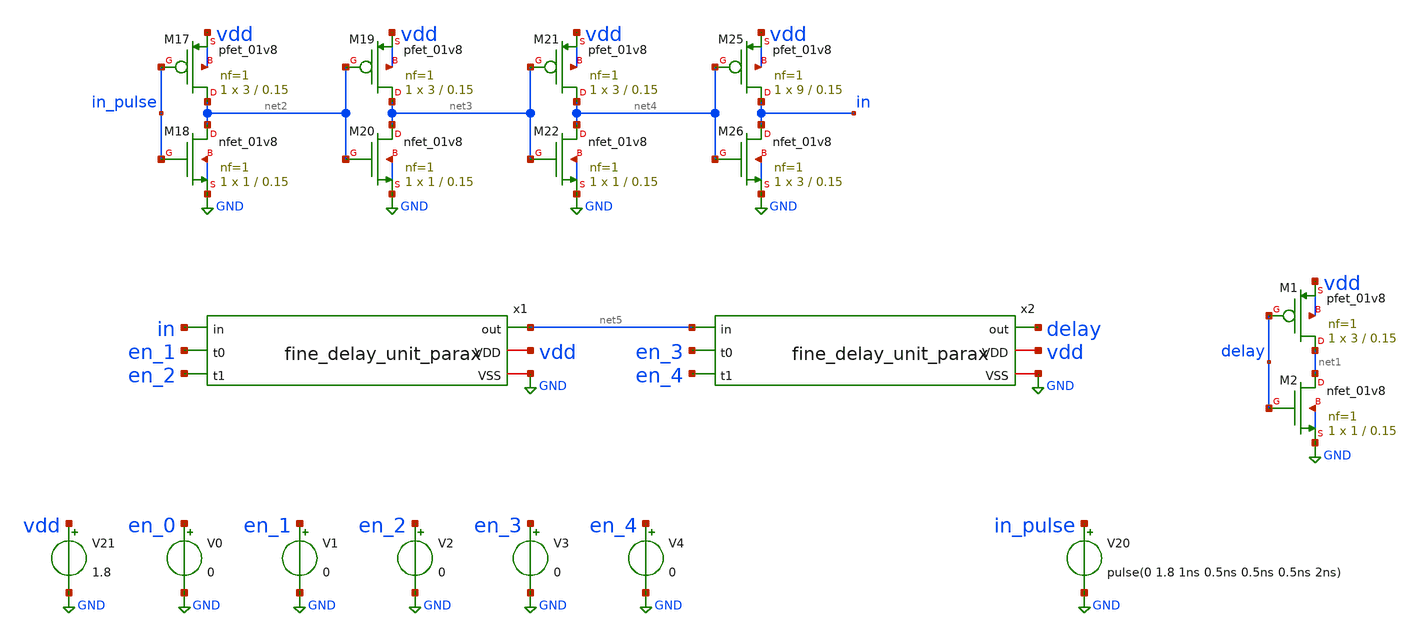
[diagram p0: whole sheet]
** sch_path: xschem/fine_delay_parax_tb.sch
**.subckt fine_delay_parax_tb
V21 vdd GND 1.8
V20 in_pulse GND pulse(0 1.8 1ns 0.5ns 0.5ns 0.5ns 2ns)
XM1 net1 delay vdd vdd sky130_fd_pr__pfet_01v8 L=0.15 W=3 nf=1 ad='int((nf+1)/2) * W/nf * 0.29' as='int((nf+2)/2) * W/nf * 0.29'
+ pd='2*int((nf+1)/2) * (W/nf + 0.29)' ps='2*int((nf+2)/2) * (W/nf + 0.29)' nrd='0.29 / W' nrs='0.29 / W'
+ sa=0 sb=0 sd=0 mult=1 m=1
XM2 net1 delay GND GND sky130_fd_pr__nfet_01v8 L=0.15 W=1 nf=1 ad='int((nf+1)/2) * W/nf * 0.29' as='int((nf+2)/2) * W/nf * 0.29'
+ pd='2*int((nf+1)/2) * (W/nf + 0.29)' ps='2*int((nf+2)/2) * (W/nf + 0.29)' nrd='0.29 / W' nrs='0.29 / W'
+ sa=0 sb=0 sd=0 mult=1 m=1
V0 en_0 GND 0
V1 en_1 GND 0
V2 en_2 GND 0
V3 en_3 GND 0
XM17 net2 in_pulse vdd vdd sky130_fd_pr__pfet_01v8 L=0.15 W=3 nf=1 ad='int((nf+1)/2) * W/nf * 0.29' as='int((nf+2)/2) * W/nf * 0.29'
+ pd='2*int((nf+1)/2) * (W/nf + 0.29)' ps='2*int((nf+2)/2) * (W/nf + 0.29)' nrd='0.29 / W' nrs='0.29 / W'
+ sa=0 sb=0 sd=0 mult=1 m=1
XM18 net2 in_pulse GND GND sky130_fd_pr__nfet_01v8 L=0.15 W=1 nf=1 ad='int((nf+1)/2) * W/nf * 0.29' as='int((nf+2)/2) * W/nf * 0.29'
+ pd='2*int((nf+1)/2) * (W/nf + 0.29)' ps='2*int((nf+2)/2) * (W/nf + 0.29)' nrd='0.29 / W' nrs='0.29 / W'
+ sa=0 sb=0 sd=0 mult=1 m=1
XM19 net3 net2 vdd vdd sky130_fd_pr__pfet_01v8 L=0.15 W=3 nf=1 ad='int((nf+1)/2) * W/nf * 0.29' as='int((nf+2)/2) * W/nf * 0.29'
+ pd='2*int((nf+1)/2) * (W/nf + 0.29)' ps='2*int((nf+2)/2) * (W/nf + 0.29)' nrd='0.29 / W' nrs='0.29 / W'
+ sa=0 sb=0 sd=0 mult=1 m=1
XM20 net3 net2 GND GND sky130_fd_pr__nfet_01v8 L=0.15 W=1 nf=1 ad='int((nf+1)/2) * W/nf * 0.29' as='int((nf+2)/2) * W/nf * 0.29'
+ pd='2*int((nf+1)/2) * (W/nf + 0.29)' ps='2*int((nf+2)/2) * (W/nf + 0.29)' nrd='0.29 / W' nrs='0.29 / W'
+ sa=0 sb=0 sd=0 mult=1 m=1
XM21 net4 net3 vdd vdd sky130_fd_pr__pfet_01v8 L=0.15 W=3 nf=1 ad='int((nf+1)/2) * W/nf * 0.29' as='int((nf+2)/2) * W/nf * 0.29'
+ pd='2*int((nf+1)/2) * (W/nf + 0.29)' ps='2*int((nf+2)/2) * (W/nf + 0.29)' nrd='0.29 / W' nrs='0.29 / W'
+ sa=0 sb=0 sd=0 mult=1 m=1
XM22 net4 net3 GND GND sky130_fd_pr__nfet_01v8 L=0.15 W=1 nf=1 ad='int((nf+1)/2) * W/nf * 0.29' as='int((nf+2)/2) * W/nf * 0.29'
+ pd='2*int((nf+1)/2) * (W/nf + 0.29)' ps='2*int((nf+2)/2) * (W/nf + 0.29)' nrd='0.29 / W' nrs='0.29 / W'
+ sa=0 sb=0 sd=0 mult=1 m=1
XM25 in net4 vdd vdd sky130_fd_pr__pfet_01v8 L=0.15 W=9 nf=1 ad='int((nf+1)/2) * W/nf * 0.29' as='int((nf+2)/2) * W/nf * 0.29'
+ pd='2*int((nf+1)/2) * (W/nf + 0.29)' ps='2*int((nf+2)/2) * (W/nf + 0.29)' nrd='0.29 / W' nrs='0.29 / W'
+ sa=0 sb=0 sd=0 mult=1 m=1
XM26 in net4 GND GND sky130_fd_pr__nfet_01v8 L=0.15 W=3 nf=1 ad='int((nf+1)/2) * W/nf * 0.29' as='int((nf+2)/2) * W/nf * 0.29'
+ pd='2*int((nf+1)/2) * (W/nf + 0.29)' ps='2*int((nf+2)/2) * (W/nf + 0.29)' nrd='0.29 / W' nrs='0.29 / W'
+ sa=0 sb=0 sd=0 mult=1 m=1
x1 in en_1 en_2 net5 vdd GND fine_delay_unit_parax
x2 net5 en_3 en_4 delay vdd GND fine_delay_unit_parax
V4 en_4 GND 0
**** begin user architecture code

** opencircuitdesign pdks install
.lib $::SKYWATER_MODELS/sky130.lib.spice tt





.control
alter V0 0
alter V1 0
alter V2 0
alter V3 0
alter V4 0

foreach i 0 1 2 3 4
alter V$i 1.8

* Run transient analysis
tran 0.0001n 5n

* Save results for this step
save v(in) v(delay)
set wr_vecnames
wrdata fine_delay_parax_tb_$i v(in) v(delay)

end
.endc


**** end user architecture code
**.ends

* expanding   symbol:  fine_delay_unit_parax.sym # of pins=6
** sym_path: xschem/fine_delay.sym
.include [file normalize ../mag/fine_delay_unit.sim.spice]
.GLOBAL GND
.end
